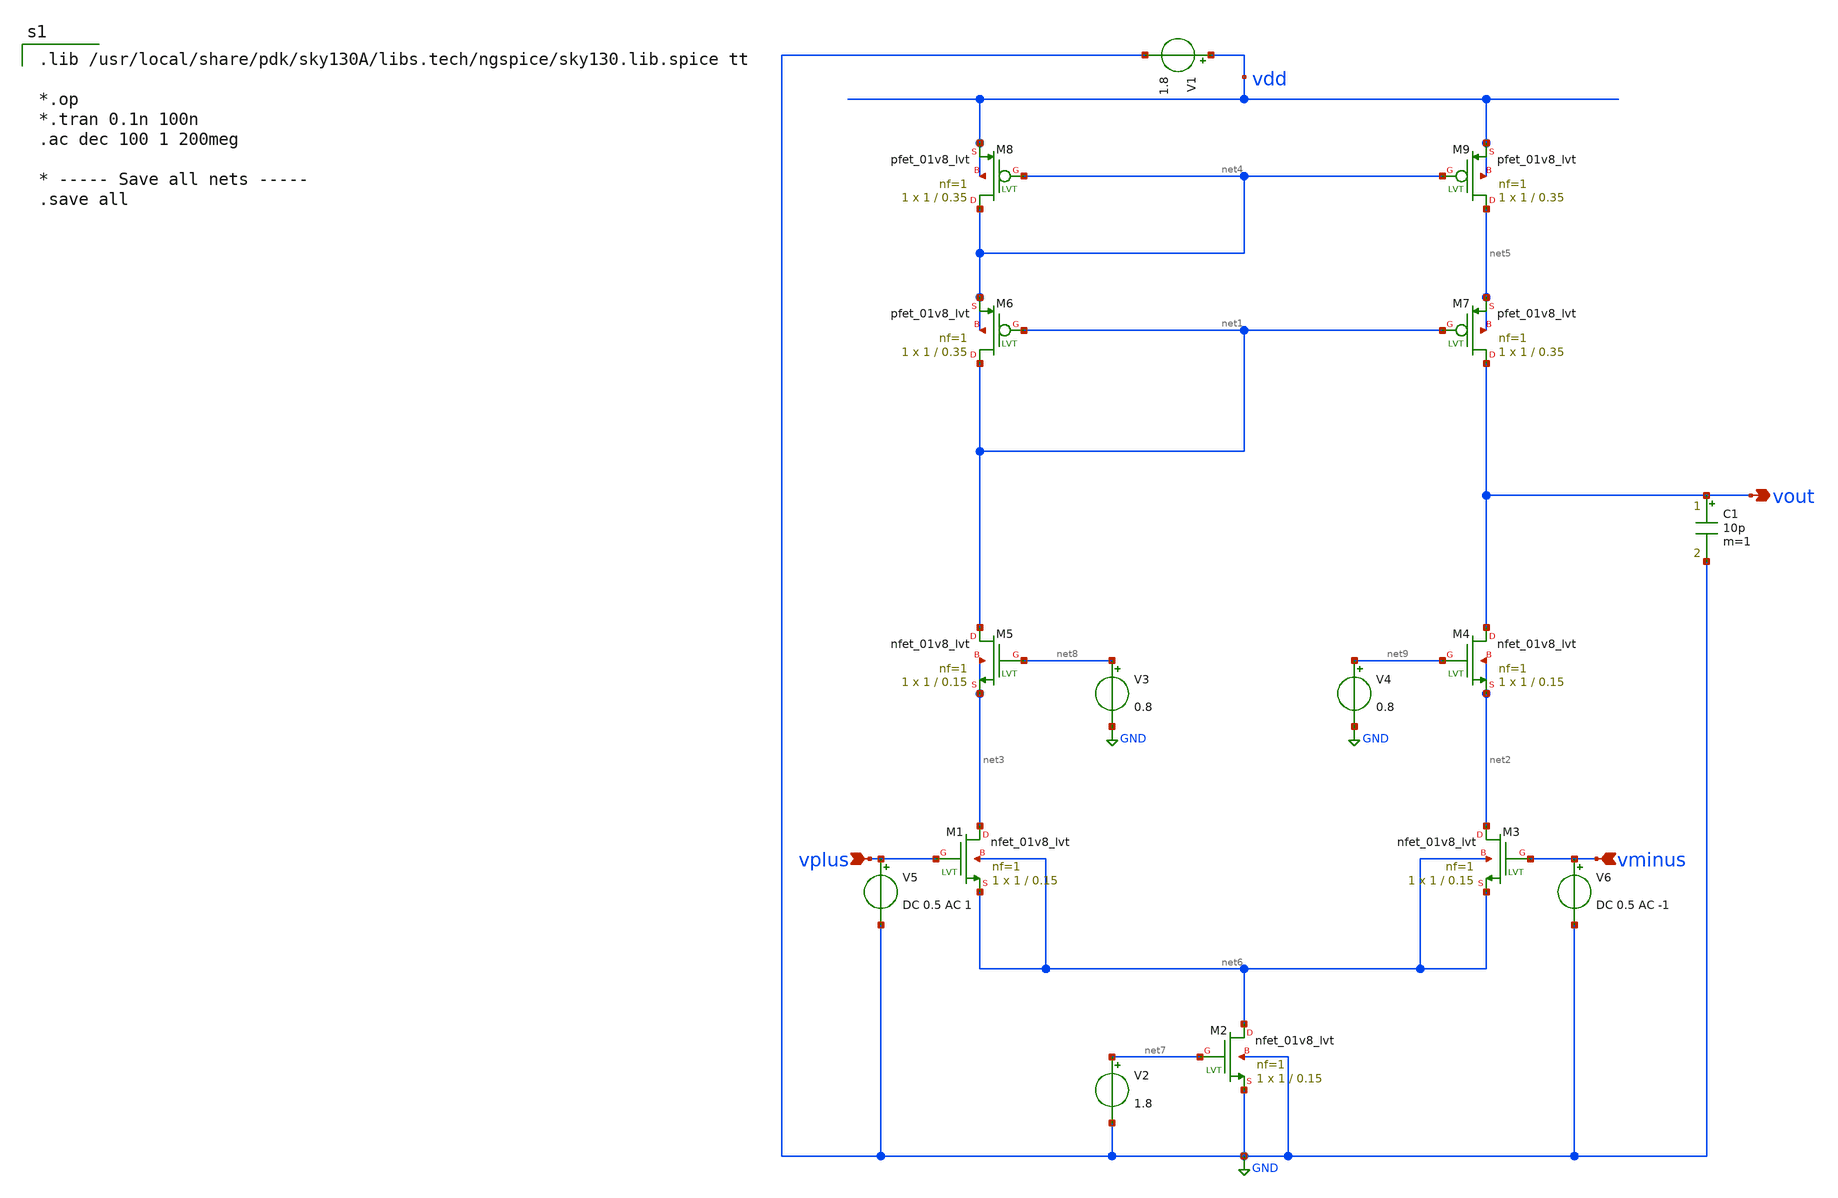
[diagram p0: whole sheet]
** sch_path: 9T_OTA_telescopic.sch
**.subckt 9T_OTA_telescopic vplus vminus vout
*.ipin vplus
*.ipin vminus
*.opin vout
C1 vout GND 10p m=1
V1 vdd GND 1.8
V2 net7 GND 1.8
V3 net8 GND 0.8
V4 net9 GND 0.8
V5 vplus GND DC 0.5 AC 1
V6 vminus GND DC 0.5 AC -1
XM1 net3 vplus net6 net6 sky130_fd_pr__nfet_01v8_lvt L=0.15 W=1 nf=1 ad='int((1 + 1)/2) * 1 / 1 * 0.29'
+ as='int((1 + 2)/2) * 1 / 1 * 0.29' pd='2*int((1 + 1)/2) * (1 / 1 + 0.29)' ps='2*int((1 + 2)/2) * (1 / 1 + 0.29)'
+ nrd='0.29 / 1 ' nrs='0.29 / 1 ' sa=0 sb=0 sd=0 mult=1 m=1
XM2 net6 net7 GND GND sky130_fd_pr__nfet_01v8_lvt L=0.15 W=1 nf=1 ad='int((1 + 1)/2) * 1 / 1 * 0.29'
+ as='int((1 + 2)/2) * 1 / 1 * 0.29' pd='2*int((1 + 1)/2) * (1 / 1 + 0.29)' ps='2*int((1 + 2)/2) * (1 / 1 + 0.29)'
+ nrd='0.29 / 1 ' nrs='0.29 / 1 ' sa=0 sb=0 sd=0 mult=1 m=1
XM3 net2 vminus net6 net6 sky130_fd_pr__nfet_01v8_lvt L=0.15 W=1 nf=1 ad='int((1 + 1)/2) * 1 / 1 * 0.29'
+ as='int((1 + 2)/2) * 1 / 1 * 0.29' pd='2*int((1 + 1)/2) * (1 / 1 + 0.29)' ps='2*int((1 + 2)/2) * (1 / 1 + 0.29)'
+ nrd='0.29 / 1 ' nrs='0.29 / 1 ' sa=0 sb=0 sd=0 mult=1 m=1
XM4 vout net9 net2 net2 sky130_fd_pr__nfet_01v8_lvt L=0.15 W=1 nf=1 ad='int((1 + 1)/2) * 1 / 1 * 0.29'
+ as='int((1 + 2)/2) * 1 / 1 * 0.29' pd='2*int((1 + 1)/2) * (1 / 1 + 0.29)' ps='2*int((1 + 2)/2) * (1 / 1 + 0.29)'
+ nrd='0.29 / 1 ' nrs='0.29 / 1 ' sa=0 sb=0 sd=0 mult=1 m=1
XM5 net1 net8 net3 net3 sky130_fd_pr__nfet_01v8_lvt L=0.15 W=1 nf=1 ad='int((1 + 1)/2) * 1 / 1 * 0.29'
+ as='int((1 + 2)/2) * 1 / 1 * 0.29' pd='2*int((1 + 1)/2) * (1 / 1 + 0.29)' ps='2*int((1 + 2)/2) * (1 / 1 + 0.29)'
+ nrd='0.29 / 1 ' nrs='0.29 / 1 ' sa=0 sb=0 sd=0 mult=1 m=1
XM6 net1 net1 net4 net4 sky130_fd_pr__pfet_01v8_lvt L=0.35 W=1 nf=1 ad='int((1 + 1)/2) * 1 / 1 * 0.29'
+ as='int((1 + 2)/2) * 1 / 1 * 0.29' pd='2*int((1 + 1)/2) * (1 / 1 + 0.29)' ps='2*int((1 + 2)/2) * (1 / 1 + 0.29)'
+ nrd='0.29 / 1 ' nrs='0.29 / 1 ' sa=0 sb=0 sd=0 mult=1 m=1
XM7 vout net1 net5 net5 sky130_fd_pr__pfet_01v8_lvt L=0.35 W=1 nf=1 ad='int((1 + 1)/2) * 1 / 1 * 0.29'
+ as='int((1 + 2)/2) * 1 / 1 * 0.29' pd='2*int((1 + 1)/2) * (1 / 1 + 0.29)' ps='2*int((1 + 2)/2) * (1 / 1 + 0.29)'
+ nrd='0.29 / 1 ' nrs='0.29 / 1 ' sa=0 sb=0 sd=0 mult=1 m=1
XM8 net4 net4 vdd vdd sky130_fd_pr__pfet_01v8_lvt L=0.35 W=1 nf=1 ad='int((1 + 1)/2) * 1 / 1 * 0.29'
+ as='int((1 + 2)/2) * 1 / 1 * 0.29' pd='2*int((1 + 1)/2) * (1 / 1 + 0.29)' ps='2*int((1 + 2)/2) * (1 / 1 + 0.29)'
+ nrd='0.29 / 1 ' nrs='0.29 / 1 ' sa=0 sb=0 sd=0 mult=1 m=1
XM9 net5 net4 vdd vdd sky130_fd_pr__pfet_01v8_lvt L=0.35 W=1 nf=1 ad='int((1 + 1)/2) * 1 / 1 * 0.29'
+ as='int((1 + 2)/2) * 1 / 1 * 0.29' pd='2*int((1 + 1)/2) * (1 / 1 + 0.29)' ps='2*int((1 + 2)/2) * (1 / 1 + 0.29)'
+ nrd='0.29 / 1 ' nrs='0.29 / 1 ' sa=0 sb=0 sd=0 mult=1 m=1
**** begin user architecture code

.lib /usr/local/share/pdk/sky130A/libs.tech/ngspice/sky130.lib.spice tt

*.op
*.tran 0.1n 100n
.ac dec 100 1 200meg

* ----- Save all nets -----
.save all

**** end user architecture code
**.ends
.GLOBAL GND
.end
